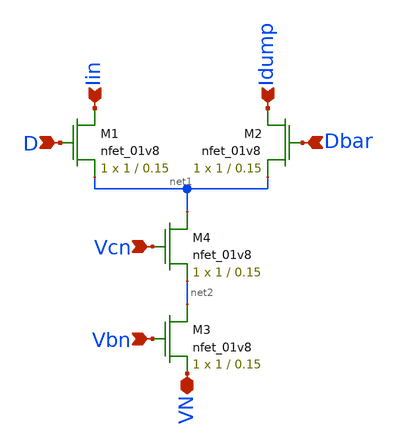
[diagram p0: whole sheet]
** sch_path: mp5/xschem/current_steering_cell.sch
**.subckt current_steering_cell VN D Dbar Vcn Iin Idump Vbn
*.iopin VN
*.ipin D
*.ipin Dbar
*.ipin Vcn
*.ipin Iin
*.ipin Idump
*.ipin Vbn
XM1 Iin D net1 GND sky130_fd_pr__nfet_01v8 L=0.15 W=1 nf=1 ad='int((nf+1)/2) * W/nf * 0.29' as='int((nf+2)/2) * W/nf * 0.29'
+ pd='2*int((nf+1)/2) * (W/nf + 0.29)' ps='2*int((nf+2)/2) * (W/nf + 0.29)' nrd='0.29 / W' nrs='0.29 / W'
+ sa=0 sb=0 sd=0 mult=1 m=1
XM2 Idump Dbar net1 GND sky130_fd_pr__nfet_01v8 L=0.15 W=1 nf=1 ad='int((nf+1)/2) * W/nf * 0.29' as='int((nf+2)/2) * W/nf * 0.29'
+ pd='2*int((nf+1)/2) * (W/nf + 0.29)' ps='2*int((nf+2)/2) * (W/nf + 0.29)' nrd='0.29 / W' nrs='0.29 / W'
+ sa=0 sb=0 sd=0 mult=1 m=1
XM3 net2 Vbn VN GND sky130_fd_pr__nfet_01v8 L=0.15 W=1 nf=1 ad='int((nf+1)/2) * W/nf * 0.29' as='int((nf+2)/2) * W/nf * 0.29'
+ pd='2*int((nf+1)/2) * (W/nf + 0.29)' ps='2*int((nf+2)/2) * (W/nf + 0.29)' nrd='0.29 / W' nrs='0.29 / W'
+ sa=0 sb=0 sd=0 mult=1 m=1
XM4 net1 Vcn net2 GND sky130_fd_pr__nfet_01v8 L=0.15 W=1 nf=1 ad='int((nf+1)/2) * W/nf * 0.29' as='int((nf+2)/2) * W/nf * 0.29'
+ pd='2*int((nf+1)/2) * (W/nf + 0.29)' ps='2*int((nf+2)/2) * (W/nf + 0.29)' nrd='0.29 / W' nrs='0.29 / W'
+ sa=0 sb=0 sd=0 mult=1 m=1
**.ends
.end
